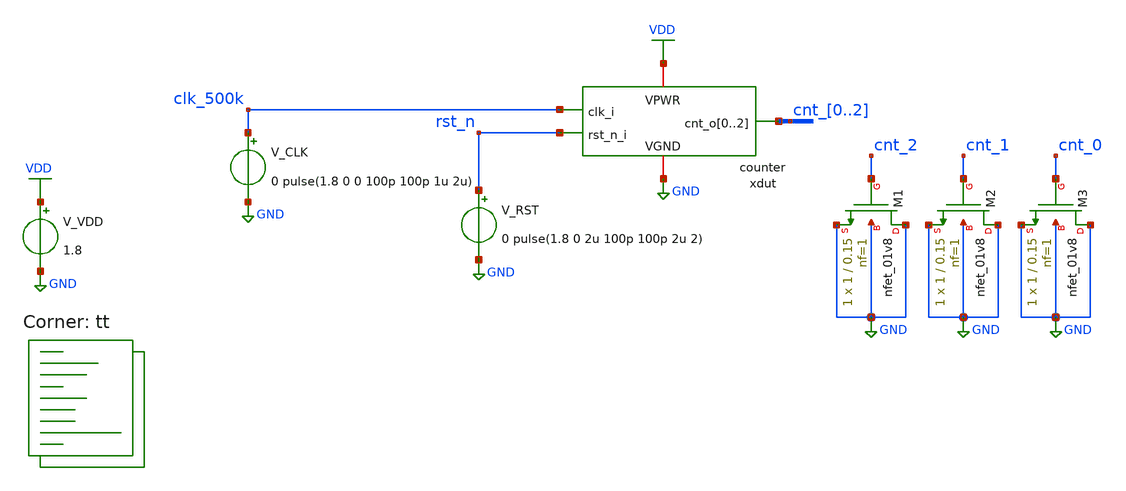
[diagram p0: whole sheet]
** sch_path: examples/3b_DAC_AMS/xschem/counter_tb.sch
**.subckt counter_tb
xdut GND VDD clk_500k cnt_0 cnt_1 cnt_2 rst_n counter
V_VDD VDD GND 1.8
V_CLK clk_500k GND 0 pulse(1.8 0 0 100p 100p 1u 2u)
V_RST rst_n GND 0 pulse(1.8 0 2u 100p 100p 2u 2)
XM1 GND cnt_2 GND GND sky130_fd_pr__nfet_01v8 L=0.15 W=1 nf=1 ad='int((nf+1)/2) * W/nf * 0.29' as='int((nf+2)/2) * W/nf * 0.29'
+ pd='2*int((nf+1)/2) * (W/nf + 0.29)' ps='2*int((nf+2)/2) * (W/nf + 0.29)' nrd='0.29 / W' nrs='0.29 / W'
+ sa=0 sb=0 sd=0 mult=1 m=1
XM2 GND cnt_1 GND GND sky130_fd_pr__nfet_01v8 L=0.15 W=1 nf=1 ad='int((nf+1)/2) * W/nf * 0.29' as='int((nf+2)/2) * W/nf * 0.29'
+ pd='2*int((nf+1)/2) * (W/nf + 0.29)' ps='2*int((nf+2)/2) * (W/nf + 0.29)' nrd='0.29 / W' nrs='0.29 / W'
+ sa=0 sb=0 sd=0 mult=1 m=1
XM3 GND cnt_0 GND GND sky130_fd_pr__nfet_01v8 L=0.15 W=1 nf=1 ad='int((nf+1)/2) * W/nf * 0.29' as='int((nf+2)/2) * W/nf * 0.29'
+ pd='2*int((nf+1)/2) * (W/nf + 0.29)' ps='2*int((nf+2)/2) * (W/nf + 0.29)' nrd='0.29 / W' nrs='0.29 / W'
+ sa=0 sb=0 sd=0 mult=1 m=1
**** begin user architecture code


* ngspice commands
****************
* True mixed signal? (xspice) or analog? (spice)
****************
.include /foss/designs/SKY130-RTL-with-Custom-Standardcell-to-GDSII/examples/3b_DAC_AMS/spice/counter.xspice
*.include /foss/designs/SKY130-RTL-with-Custom-Standardcell-to-GDSII/examples/3b_DAC_AMS/spice/counter.spice

.save all
.control
set num_threads=12
tran 10n 20u

write counter_tb.raw

.endc


.lib $::SKYWATER_MODELS/sky130.lib.spice tt
**** end user architecture code
**.ends
.GLOBAL GND
.GLOBAL VDD
.end
